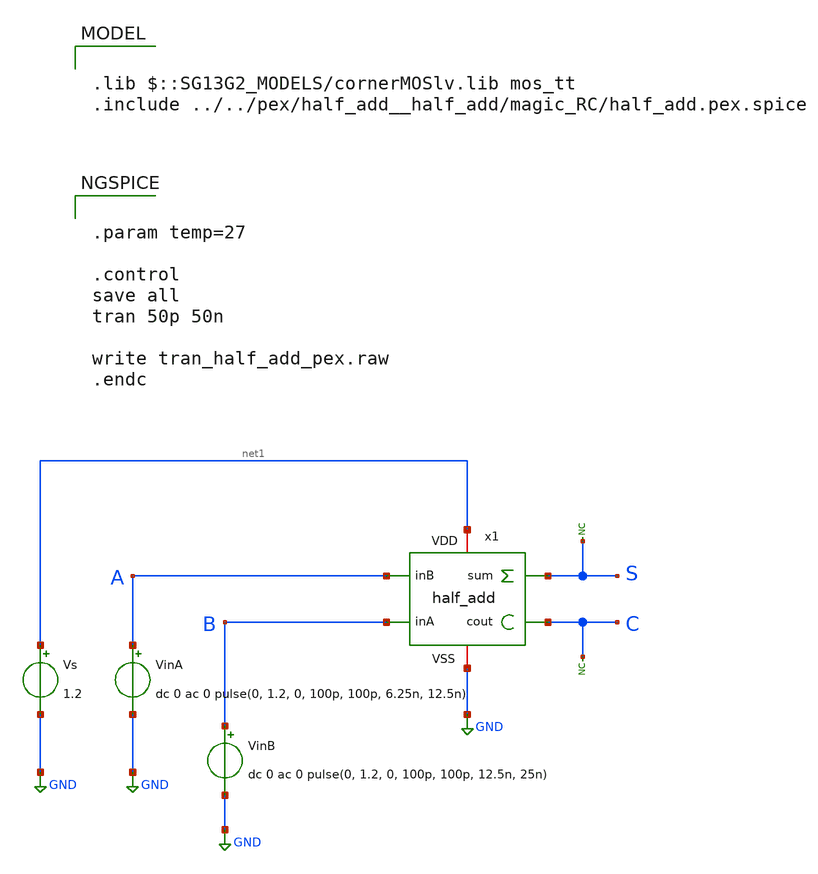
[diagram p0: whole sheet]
** sch_path: Combined_Design/design_data/xschem/half_add_pex_tb.sch

.lib $::SG13G2_MODELS/cornerMOSlv.lib mos_tt
.include ../../pex/half_add__half_add/magic_RC/half_add.pex.spice

**.subckt half_add_pex_tb
VinA A GND dc 0 ac 0 pulse(0, 1.2, 0, 100p, 100p, 6.25n, 12.5n)
VinB B GND dc 0 ac 0 pulse(0, 1.2, 0, 100p, 100p, 12.5n, 25n)
Vs net1 GND 1.2
* noconn S
* noconn C
x1 A S B net1 GND C half_add
**** begin user architecture code


.param temp=27

.control
save all
tran 50p 50n

write tran_half_add_pex.raw
.endc


**** end user architecture code
**.ends
.GLOBAL GND
.end
